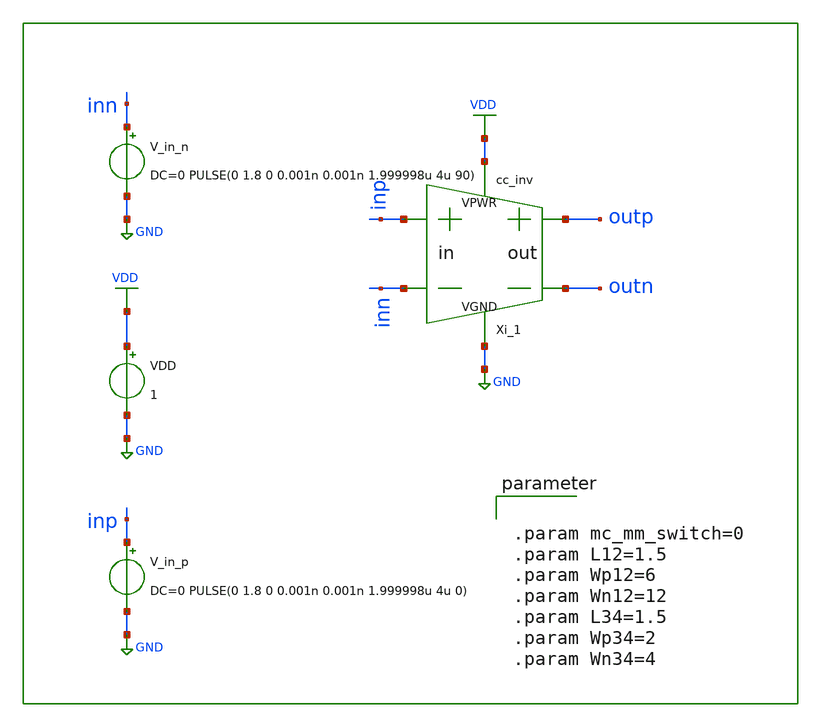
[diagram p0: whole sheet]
** sch_path: circuit_model/tb/test_cc_inv.sch
**.subckt test_cc_inv
Xi_1 inp inn VDD GND outp outn cc_inv L12="L12" Wp12="Wp12" Wn12="Wn12" L34="L34" Wp34="Wp34"
+ Wn34="Wn34"
VDD VDD GND 1
V_in_p inp GND DC=0 PULSE(0 1.8 0 0.001n 0.001n 1.999998u 4u 0)
V_in_n inn GND DC=0 PULSE(0 1.8 0 0.001n 0.001n 1.999998u 4u 90)
**** begin user architecture code


.control
set nobreak
set num_thread = 5
TRAN 1n 10u

.endc




.param mc_mm_switch=0
.param L12=1.5
.param Wp12=6
.param Wn12=12
.param L34=1.5
.param Wp34=2
.param Wn34=4




.lib /home/dkits/efabless/mpw-5/pdks/sky130A/libs.tech/ngspice/sky130.lib.spice tt
.inc /home/dkits/efabless/mpw-5/pdks/sky130A/libs.ref/sky130_fd_sc_hd/spice/sky130_fd_sc_hd.spice



**** end user architecture code
**.ends

* expanding   symbol:  /home/userdata/k63D/toind_63d/Desktop/project/circuit_model/lib/cc_inv.sym #
*+ of pins=6
** sym_path: circuit_model/lib/cc_inv.sym
** sch_path: circuit_model/lib/cc_inv.sch
.subckt cc_inv inp inn VPWR VGND outp outn  L12=0.15 Wp12=1.2 Wn12=0.65 L34=0.15 Wp34=1.2 Wn34=0.65
*.opin outp
*.ipin inn
*.iopin VGND
*.opin outn
*.ipin inp
*.iopin VPWR
Xi_1 inp VPWR VGND outp inverter L="L12" Wp="Wp12" Np=1 Wn="Wn12" Nn=1
Xi_3 outp VPWR VGND outn inverter L="L34" Wp="Wp34" Np=1 Wn="Wn34" Nn=1
Xi_2 inn VPWR VGND outn inverter L="L12" Wp="Wp12" Np=1 Wn="Wn12" Nn=1
Xi_4 outn VPWR VGND outp inverter L="L34" Wp="Wp34" Np=1 Wn="Wn34" Nn=1
.ends


* expanding   symbol:  inverter.sym # of pins=4
** sym_path: circuit_model/lib/inverter.sym
** sch_path: circuit_model/lib/inverter.sch
.subckt inverter A VPWR VGND Y  L=0.15 Wp=1.2 Np=1 Wn=0.65 Nn=1
*.iopin VPWR
*.iopin VGND
*.ipin A
*.opin Y
XM1 Y A VPWR VDD sky130_fd_pr__pfet_01v8 L="L" W="Wp" nf="Np" ad='int(("Np" + 1)/2) * "Wp" / "Np" * 0.29'
+ as='int(("Np" + 2)/2) * "Wp" / "Np" * 0.29' pd='2*int(("Np" + 1)/2) * ("Wp" / "Np" + 0.29)' ps='2*int(("Np" + 2)/2) * ("Wp" / "Np" + 0.29)'
+ nrd='0.29 / "Wp" ' nrs='0.29 / "Wp" ' sa=0 sb=0 sd=0 mult=1 m=1
XM2 Y A VGND GND sky130_fd_pr__nfet_01v8 L="L" W="Wn" nf="Nn" ad='int((nf+1)/2) * W/nf * 0.29' as='int((nf+2)/2) * W/nf * 0.29'
+ pd='2*int((nf+1)/2) * (W/nf + 0.29)' ps='2*int((nf+2)/2) * (W/nf + 0.29)' nrd='0.29 / W' nrs='0.29 / W'
+ sa=0 sb=0 sd=0 mult=1 m=1
.ends

.GLOBAL VDD
.GLOBAL GND
.end
